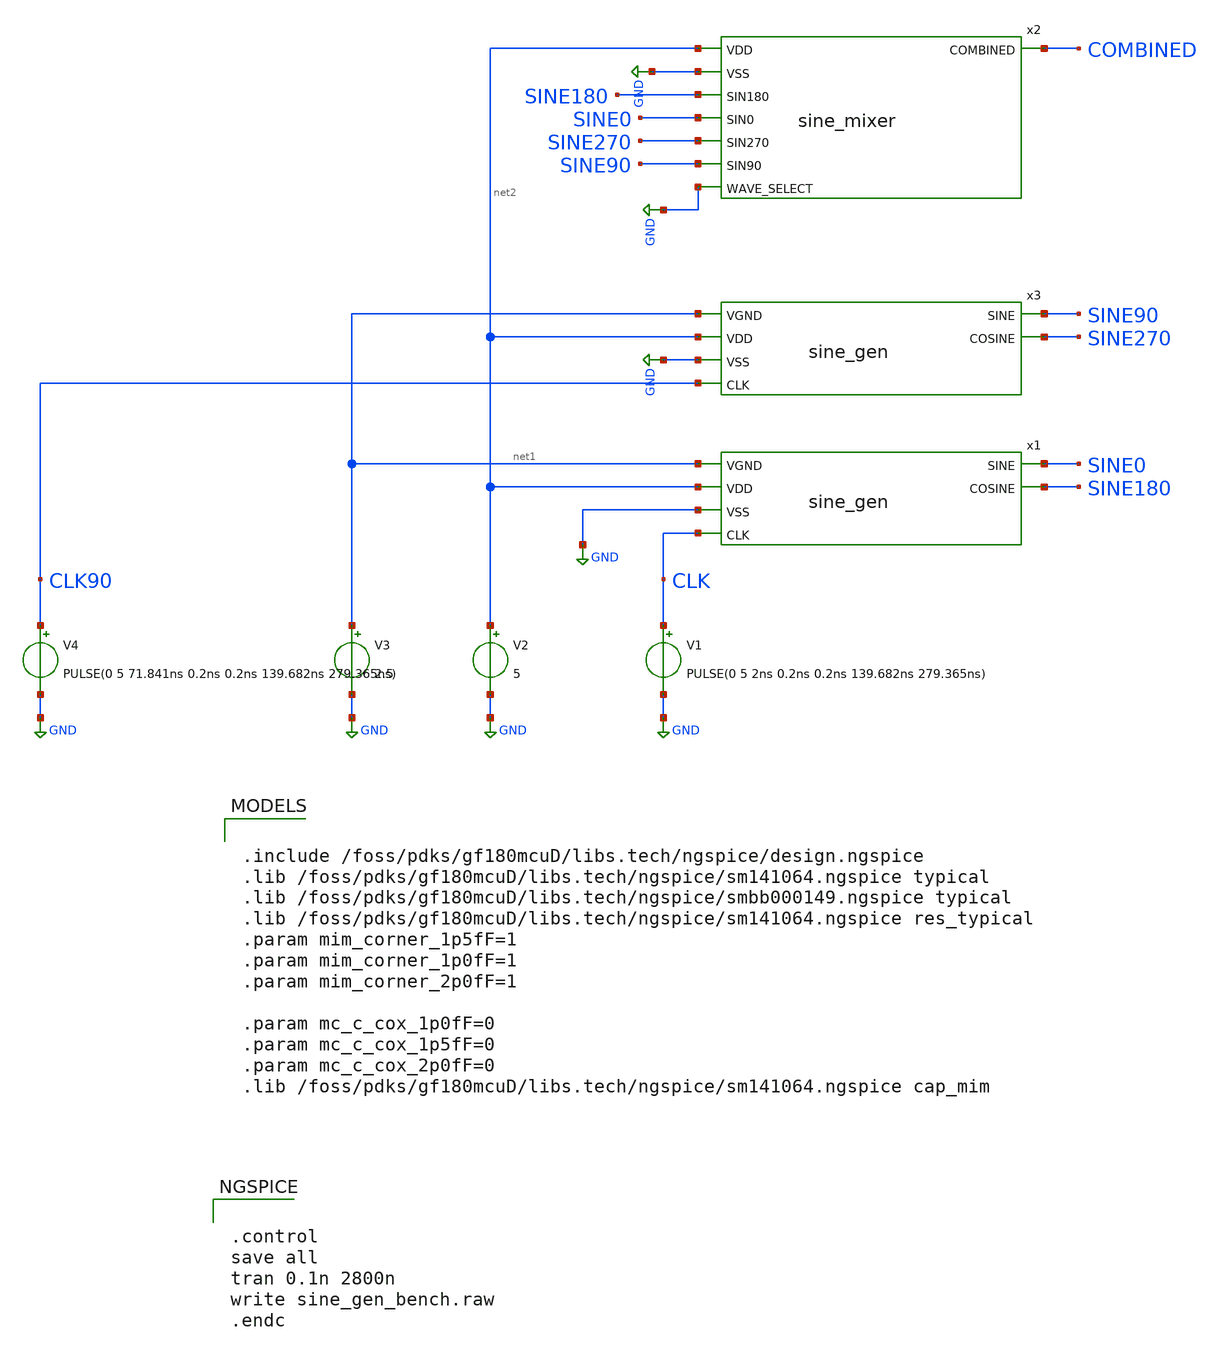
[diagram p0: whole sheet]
** sch_path: macros/Analog/gf180_ntsc/sine_gen_bench.sch
**.subckt sine_gen_bench
V1 CLK GND PULSE(0 5 2ns 0.2ns 0.2ns 139.682ns 279.365ns)
V2 net2 GND 5
V3 net1 GND 2.5
x1 net1 net2 SINE0 GND CLK SINE180 sine_gen
x2 net2 GND SINE180 SINE0 COMBINED SINE270 SINE90 GND sine_mixer
x3 net1 net2 SINE90 GND CLK90 SINE270 sine_gen
V4 CLK90 GND PULSE(0 5 71.841ns 0.2ns 0.2ns 139.682ns 279.365ns)
**** begin user architecture code

.include /foss/pdks/gf180mcuD/libs.tech/ngspice/design.ngspice
.lib /foss/pdks/gf180mcuD/libs.tech/ngspice/sm141064.ngspice typical
.lib /foss/pdks/gf180mcuD/libs.tech/ngspice/smbb000149.ngspice typical
.lib /foss/pdks/gf180mcuD/libs.tech/ngspice/sm141064.ngspice res_typical
.param mim_corner_1p5fF=1
.param mim_corner_1p0fF=1
.param mim_corner_2p0fF=1

.param mc_c_cox_1p0fF=0
.param mc_c_cox_1p5fF=0
.param mc_c_cox_2p0fF=0
.lib /foss/pdks/gf180mcuD/libs.tech/ngspice/sm141064.ngspice cap_mim



.control
save all
tran 0.1n 2800n
write sine_gen_bench.raw
.endc


**** end user architecture code
**.ends
.GLOBAL GND
.end
